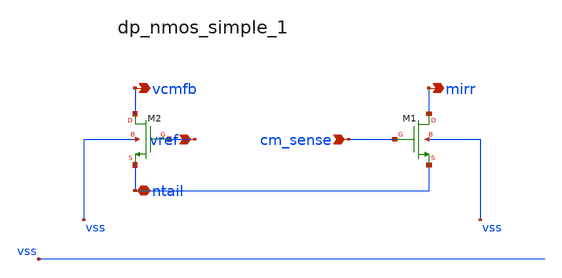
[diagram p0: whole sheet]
** sch_path: analog-db/raw/cmfb_003_5t_nmos_input/hier/blocks/dp_nmos_simple_1.sch
**.subckt dp_nmos_simple_1 vref cm_sense ntail vcmfb mirr
*.ipin vref
*.ipin cm_sense
*.iopin ntail
*.opin vcmfb
*.opin mirr
XM1 mirr cm_sense ntail vss sg13_lv_nmos w=x_dut_xm1_w l=x_dut_xm1_l ng=1 m=x_dut_xm1_m
XM2 vcmfb vref ntail vss sg13_lv_nmos w=x_dut_xm2_w l=x_dut_xm2_l ng=1 m=x_dut_xm2_m
**.ends
.end
